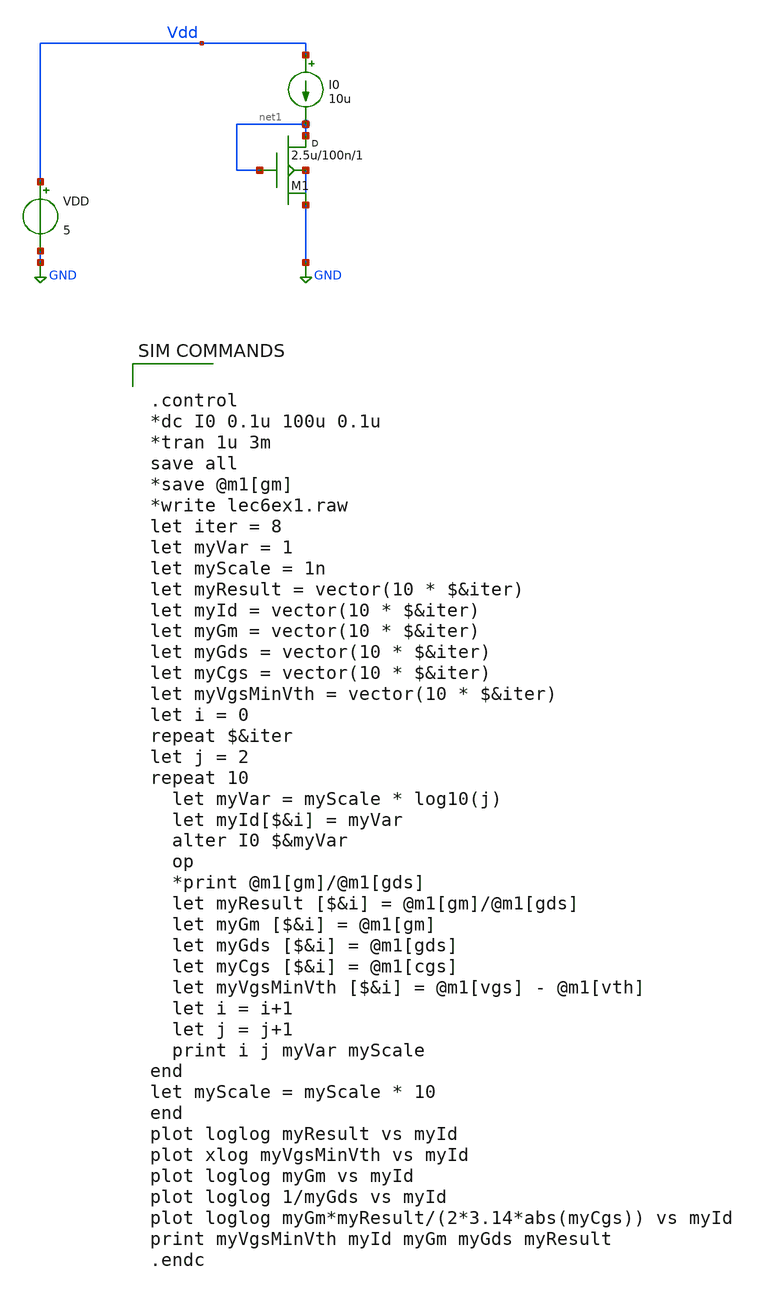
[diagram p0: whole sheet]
** sch_path: hw6.sch
**.subckt hw6
VDD Vdd GND 5
I0 Vdd net1 10u
M1 net1 net1 GND GND N_50n w=2.5u l=100n m=1
**** begin user architecture code


.control
*dc I0 0.1u 100u 0.1u
*tran 1u 3m
save all
*save @m1[gm]
*write lec6ex1.raw
let iter = 8
let myVar = 1
let myScale = 1n
let myResult = vector(10 * $&iter)
let myId = vector(10 * $&iter)
let myGm = vector(10 * $&iter)
let myGds = vector(10 * $&iter)
let myCgs = vector(10 * $&iter)
let myVgsMinVth = vector(10 * $&iter)
let i = 0
repeat $&iter
let j = 2
repeat 10
  let myVar = myScale * log10(j)
  let myId[$&i] = myVar
  alter I0 $&myVar
  op
  *print @m1[gm]/@m1[gds]
  let myResult [$&i] = @m1[gm]/@m1[gds]
  let myGm [$&i] = @m1[gm]
  let myGds [$&i] = @m1[gds]
  let myCgs [$&i] = @m1[cgs]
  let myVgsMinVth [$&i] = @m1[vgs] - @m1[vth]
  let i = i+1
  let j = j+1
  print i j myVar myScale
end
let myScale = myScale * 10
end
plot loglog myResult vs myId
plot xlog myVgsMinVth vs myId
plot loglog myGm vs myId
plot loglog 1/myGds vs myId
plot loglog myGm*myResult/(2*3.14*abs(myCgs)) vs myId
print myVgsMinVth myId myGm myGds myResult
.endc




*

* Long channel models from CMOS Circuit Design, Layout, and Simulation,

* Level=3 models VDD=5V, see CMOSedu.com

*

.MODEL N_1u NMOS LEVEL  = 3
  TOX    = 200E-10         NSUB   = 1E17            GAMMA  = 0.5
  PHI    = 0.7             VTO    = 0.8             DELTA  = 3.0
  UO     = 650             ETA    = 3.0E-6          THETA  = 0.1
  KP     = 120E-6          VMAX   = 1E5             KAPPA  = 0.3
  RSH    = 0               NFS    = 1E12            TPG    = 1
  XJ     = 500E-9          LD     = 100E-9
  CGDO   = 200E-12         CGSO   = 200E-12         CGBO   = 1E-10
  CJ     = 400E-6          PB     = 1               MJ     = 0.5
  CJSW   = 300E-12         MJSW   = 0.5

*

.MODEL P_1u PMOS LEVEL  = 3
  TOX    = 200E-10         NSUB   = 1E17            GAMMA  = 0.6
  PHI    = 0.7             VTO    = -0.9            DELTA  = 0.1
  UO     = 250             ETA    = 0               THETA  = 0.1
  KP     = 40E-6           VMAX   = 5E4             KAPPA  = 1
  RSH    = 0               NFS    = 1E12            TPG    = -1
  XJ     = 500E-9          LD     = 100E-9
  CGDO   = 200E-12         CGSO   = 200E-12         CGBO   = 1E-10
  CJ     = 400E-6          PB     = 1               MJ     = 0.5
  CJSW   = 300E-12         MJSW   = 0.5

*

*

* Short channel models from CMOS Circuit Design, Layout, and Simulation,

* 50nm BSIM4 models VDD=1V, see CMOSedu.com

*

.model  N_50n  nmos  level = 54
 binunit = 1            paramchk= 1            mobmod  = 0
 capmod  = 2            igcmod  = 1            igbmod  = 1            geomod  = 0
 diomod  = 1            rdsmod  = 0            rbodymod= 1            rgatemod= 1
 permod  = 1            acnqsmod= 0            trnqsmod= 0
 tnom    = 27           toxe    = 1.4e-009     toxp    = 7e-010       toxm    = 1.4e-009
 epsrox  = 3.9          wint    = 5e-009       lint    = 1.2e-008
 ll      = 0            wl      = 0            lln     = 1            wln     = 1
 lw      = 0            ww      = 0            lwn     = 1            wwn     = 1
 lwl     = 0            wwl     = 0            xpart   = 0            toxref  = 1.4e-009
 vth0    = 0.22         k1      = 0.35         k2      = 0.05         k3      = 0
 k3b     = 0            w0      = 2.5e-006     dvt0    = 2.8          dvt1    = 0.52
 dvt2    = -0.032       dvt0w   = 0            dvt1w   = 0            dvt2w   = 0
 dsub    = 2            minv    = 0.05         voffl   = 0            dvtp0   = 1e-007
 dvtp1   = 0.05         lpe0    = 5.75e-008    lpeb    = 2.3e-010     xj      = 2e-008
 ngate   = 5e+020       ndep    = 2.8e+018     nsd     = 1e+020       phin    = 0
 cdsc    = 0.0002       cdscb   = 0            cdscd   = 0            cit     = 0
 voff    = -0.15        nfactor = 1.2          eta0    = 0.15         etab    = 0
 vfb     = -0.55        u0      = 0.032        ua      = 1.6e-010     ub      = 1.1e-017
 uc      = -3e-011      vsat    = 1.1e+005     a0      = 2            ags     = 1e-020
 a1      = 0            a2      = 1            b0      = -1e-020      b1      = 0
 keta    = 0.04         dwg     = 0            dwb     = 0            pclm    = 0.18
 pdiblc1 = 0.028        pdiblc2 = 0.022        pdiblcb = -0.005       drout   = 0.45
 pvag    = 1e-020       delta   = 0.01         pscbe1  = 8.14e+008    pscbe2  = 1e-007
 fprout  = 0.2          pdits   = 0.2          pditsd  = 0.23         pditsl  = 2.3e+006
 rsh     = 3            rdsw    = 150          rsw     = 150          rdw     = 150
 rdswmin = 0            rdwmin  = 0            rswmin  = 0            prwg    = 0
 prwb    = 6.8e-011     wr      = 1            alpha0  = 0.074        alpha1  = 0.005
 beta0   = 30           agidl   = 0.0002       bgidl   = 2.1e+009     cgidl   = 0.0002
 egidl   = 0.8
 aigbacc = 0.012        bigbacc = 0.0028       cigbacc = 0.002
 nigbacc = 1            aigbinv = 0.014        bigbinv = 0.004        cigbinv = 0.004
 eigbinv = 1.1          nigbinv = 3            aigc    = 0.017        bigc    = 0.0028
 cigc    = 0.002        aigsd   = 0.017        bigsd   = 0.0028       cigsd   = 0.002
 nigc    = 1            poxedge = 1            pigcd   = 1            ntox    = 1
 xrcrg1  = 12           xrcrg2  = 5
 cgso    = 6.238e-010   cgdo    = 6.238e-010   cgbo    = 2.56e-011    cgdl    = 2.495e-10
 cgsl    = 2.495e-10    ckappas = 0.02         ckappad = 0.02         acde    = 1
 moin    = 15           noff    = 0.9          voffcv  = 0.02
 kt1     = -0.21        kt1l    = 0.0           kt2     = -0.042        ute     = -1.5
 ua1     = 1e-009       ub1     = -3.5e-019     uc1     = 0             prt     = 0
 at      = 53000
 fnoimod = 1            tnoimod = 0
 jss     = 0.0001       jsws    = 1e-011       jswgs   = 1e-010       njs     = 1
 ijthsfwd= 0.01         ijthsrev= 0.001        bvs     = 10           xjbvs   = 1
 jsd     = 0.0001       jswd    = 1e-011       jswgd   = 1e-010       njd     = 1
 ijthdfwd= 0.01         ijthdrev= 0.001        bvd     = 10           xjbvd   = 1
 pbs     = 1            cjs     = 0.0005       mjs     = 0.5          pbsws   = 1
 cjsws   = 5e-010       mjsws   = 0.33         pbswgs  = 1            cjswgs  = 5e-010
 mjswgs  = 0.33         pbd     = 1            cjd     = 0.0005       mjd     = 0.5
 pbswd   = 1            cjswd   = 5e-010       mjswd   = 0.33         pbswgd  = 1
 cjswgd  = 5e-010       mjswgd  = 0.33         tpb     = 0.005        tcj     = 0.001
 tpbsw   = 0.005        tcjsw   = 0.001        tpbswg  = 0.005        tcjswg  = 0.001
 xtis    = 3            xtid    = 3
 dmcg    = 0e-006       dmci    = 0e-006       dmdg    = 0e-006       dmcgt   = 0e-007
 dwj     = 0e-008     	xgw     = 0e-007       xgl     = 0e-008
 rshg    = 0.4          gbmin   = 1e-010       rbpb    = 5            rbpd    = 15
 rbps    = 15           rbdb    = 15           rbsb    = 15           ngcon   = 1

*

.model  P_50n  pmos  level = 54
 binunit = 1            paramchk= 1            mobmod  = 0
 capmod  = 2            igcmod  = 1            igbmod  = 1            geomod  = 0
 diomod  = 1            rdsmod  = 0            rbodymod= 1            rgatemod= 1
 permod  = 1            acnqsmod= 0            trnqsmod= 0
 tnom    = 27           toxe    = 1.4e-009     toxp    = 7e-010       toxm    = 1.4e-009
 epsrox  = 3.9          wint    = 5e-009       lint    = 1.2e-008
 ll      = 0            wl      = 0            lln     = 1            wln     = 1
 lw      = 0            ww      = 0            lwn     = 1            wwn     = 1
 lwl     = 0            wwl     = 0            xpart   = 0            toxref  = 1.4e-009
 vth0    = -0.22        k1      = 0.39         k2      = 0.05         k3      = 0
 k3b     = 0            w0      = 2.5e-006     dvt0    = 3.9          dvt1    = 0.635
 dvt2    = -0.032       dvt0w   = 0            dvt1w   = 0            dvt2w   = 0
 dsub    = 0.7          minv    = 0.05         voffl   = 0            dvtp0   = 0.5e-008
 dvtp1   = 0.05         lpe0    = 5.75e-008    lpeb    = 2.3e-010     xj      = 2e-008
 ngate   = 5e+020       ndep    = 2.8e+018     nsd     = 1e+020       phin    = 0
 cdsc    = 0.000258     cdscb   = 0            cdscd   = 6.1e-008     cit     = 0
 voff    = -0.15        nfactor = 2            eta0    = 0.15         etab    = 0
 vfb     = 0.55         u0      = 0.0095       ua      = 1.6e-009     ub      = 8e-018
 uc      = 4.6e-013     vsat    = 90000        a0      = 1.2          ags     = 1e-020
 a1      = 0            a2      = 1            b0      = -1e-020      b1      = 0
 keta    = -0.047       dwg     = 0            dwb     = 0            pclm    = 0.55
 pdiblc1 = 0.03         pdiblc2 = 0.0055       pdiblcb = 3.4e-008     drout   = 0.56
 pvag    = 1e-020       delta   = 0.014        pscbe1  = 8.14e+008    pscbe2  = 9.58e-007
 fprout  = 0.2          pdits   = 0.2          pditsd  = 0.23         pditsl  = 2.3e+006
 rsh     = 3            rdsw    = 250          rsw     = 160          rdw     = 160
 rdswmin = 0            rdwmin  = 0            rswmin  = 0            prwg    = 3.22e-008
 prwb    = 6.8e-011     wr      = 1            alpha0  = 0.074        alpha1  = 0.005
 beta0   = 30           agidl   = 0.0002       bgidl   = 2.1e+009     cgidl   = 0.0002
 egidl   = 0.8
 aigbacc = 0.012        bigbacc = 0.0028       cigbacc = 0.002
 nigbacc = 1            aigbinv = 0.014        bigbinv = 0.004        cigbinv = 0.004
 eigbinv = 1.1          nigbinv = 3            aigc    = 0.69         bigc    = 0.0012
 cigc    = 0.0008       aigsd   = 0.0087       bigsd   = 0.0012       cigsd   = 0.0008
 nigc    = 1            poxedge = 1            pigcd   = 1            ntox    = 1
 xrcrg1  = 12           xrcrg2  = 5
 cgso    = 7.43e-010    cgdo    = 7.43e-010    cgbo    = 2.56e-011    cgdl    = 1e-014
 cgsl    = 1e-014       ckappas = 0.5          ckappad = 0.5          acde    = 1
 moin    = 15           noff    = 0.9          voffcv  = 0.02
 kt1     = -0.19        kt1l    = 0            kt2     = -0.052        ute     = -1.5
 ua1     = -1e-009      ub1     = 2e-018       uc1     = 0             prt     = 0
 at      = 33000
 fnoimod = 1            tnoimod = 0
 jss     = 0.0001       jsws    = 1e-011       jswgs   = 1e-010       njs     = 1
 ijthsfwd= 0.01         ijthsrev= 0.001        bvs     = 10           xjbvs   = 1
 jsd     = 0.0001       jswd    = 1e-011       jswgd   = 1e-010       njd     = 1
 ijthdfwd= 0.01         ijthdrev= 0.001        bvd     = 10           xjbvd   = 1
 pbs     = 1            cjs     = 0.0005       mjs     = 0.5          pbsws   = 1
 cjsws   = 5e-010       mjsws   = 0.33         pbswgs  = 1            cjswgs  = 5e-010
 mjswgs  = 0.33         pbd     = 1            cjd     = 0.0005       mjd     = 0.5
 pbswd   = 1            cjswd   = 5e-010       mjswd   = 0.33         pbswgd  = 1
 cjswgd  = 5e-010       mjswgd  = 0.33         tpb     = 0.005        tcj     = 0.001
 tpbsw   = 0.005        tcjsw   = 0.001        tpbswg  = 0.005        tcjswg  = 0.001
 xtis    = 3            xtid    = 3
 dmcg    = 0e-006       dmci    = 0e-006       dmdg    = 0e-006       dmcgt   = 0e-007
 dwj     = 0e-008     	xgw     = 0e-007       xgl     = 0e-008
 rshg    = 0.4          gbmin   = 1e-010       rbpb    = 5            rbpd    = 15
 rbps    = 15           rbdb    = 15           rbsb    = 15           ngcon   = 1


**** end user architecture code
**.ends
.GLOBAL GND
.end
